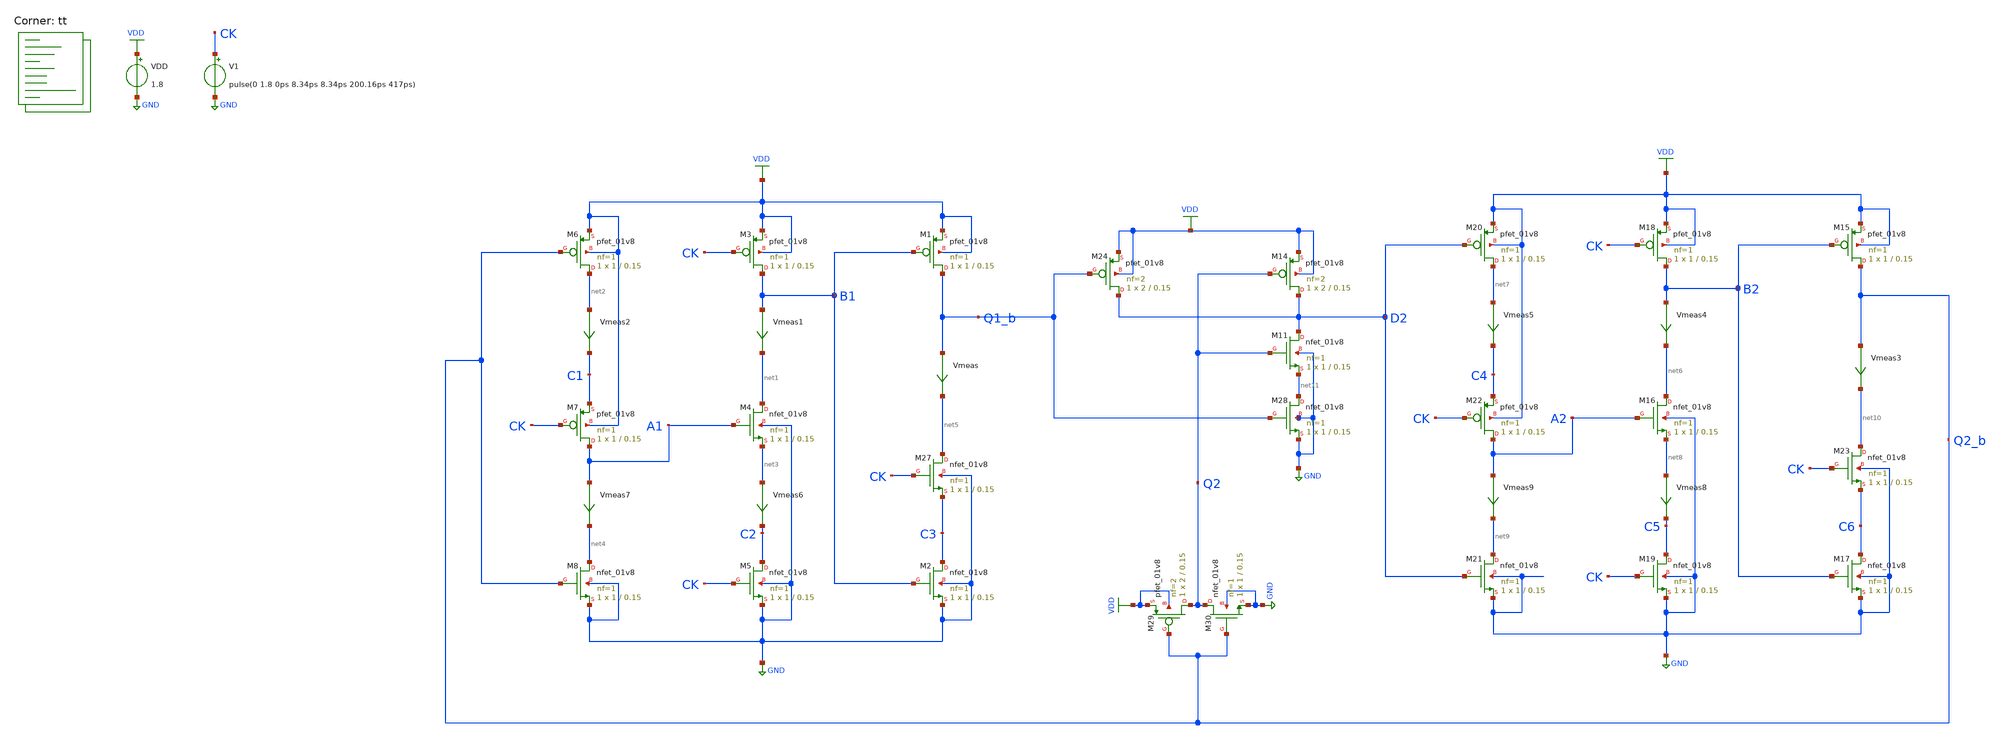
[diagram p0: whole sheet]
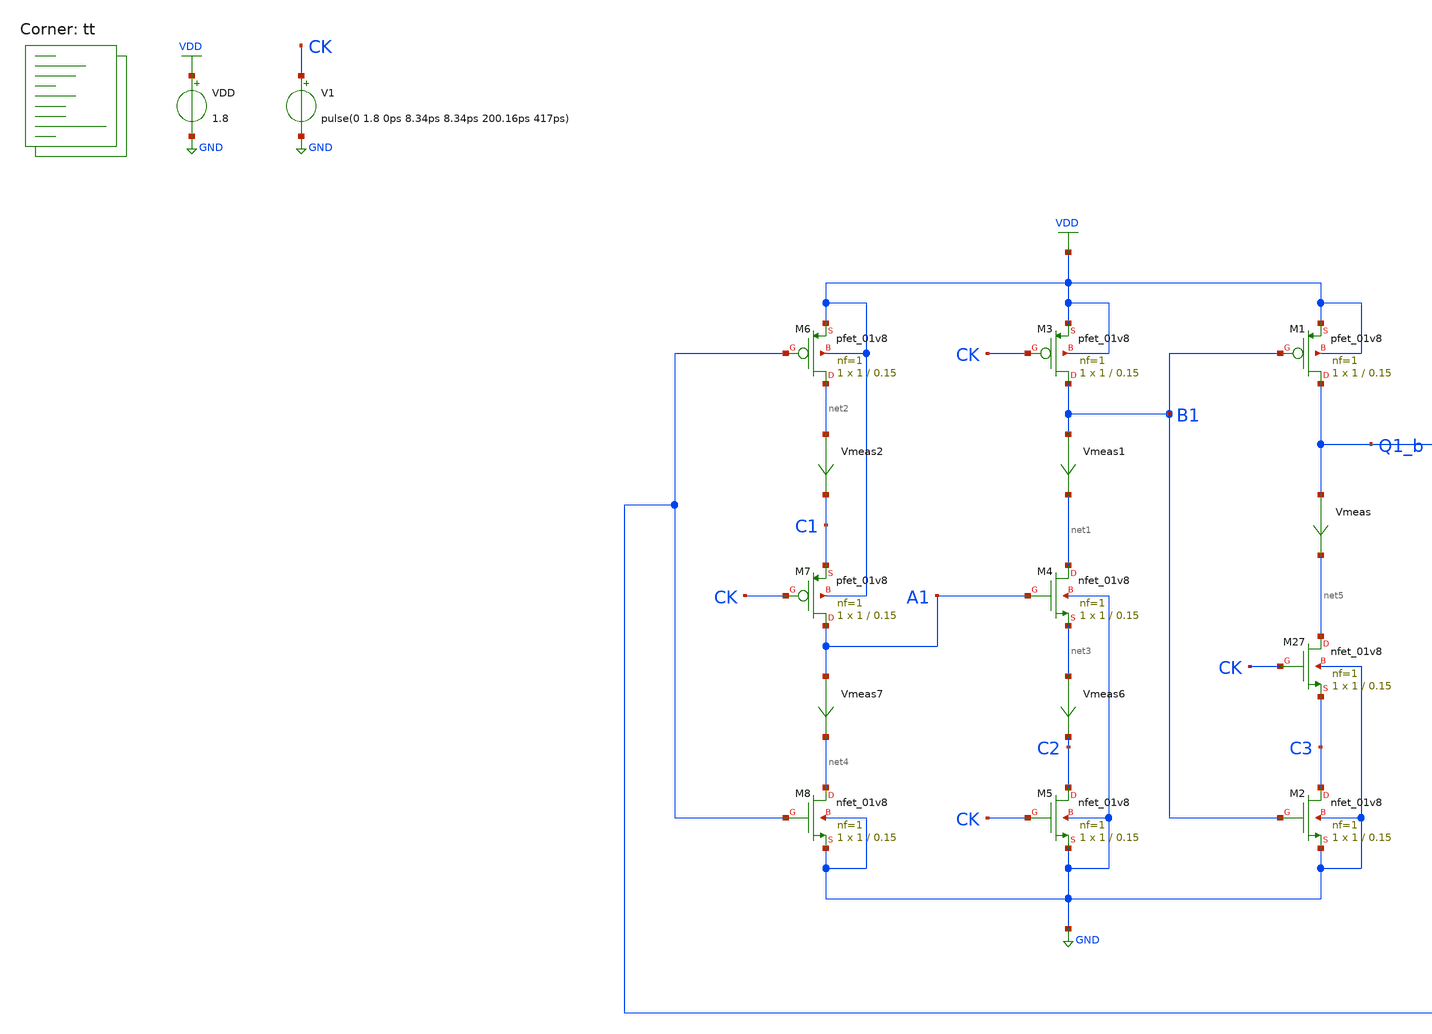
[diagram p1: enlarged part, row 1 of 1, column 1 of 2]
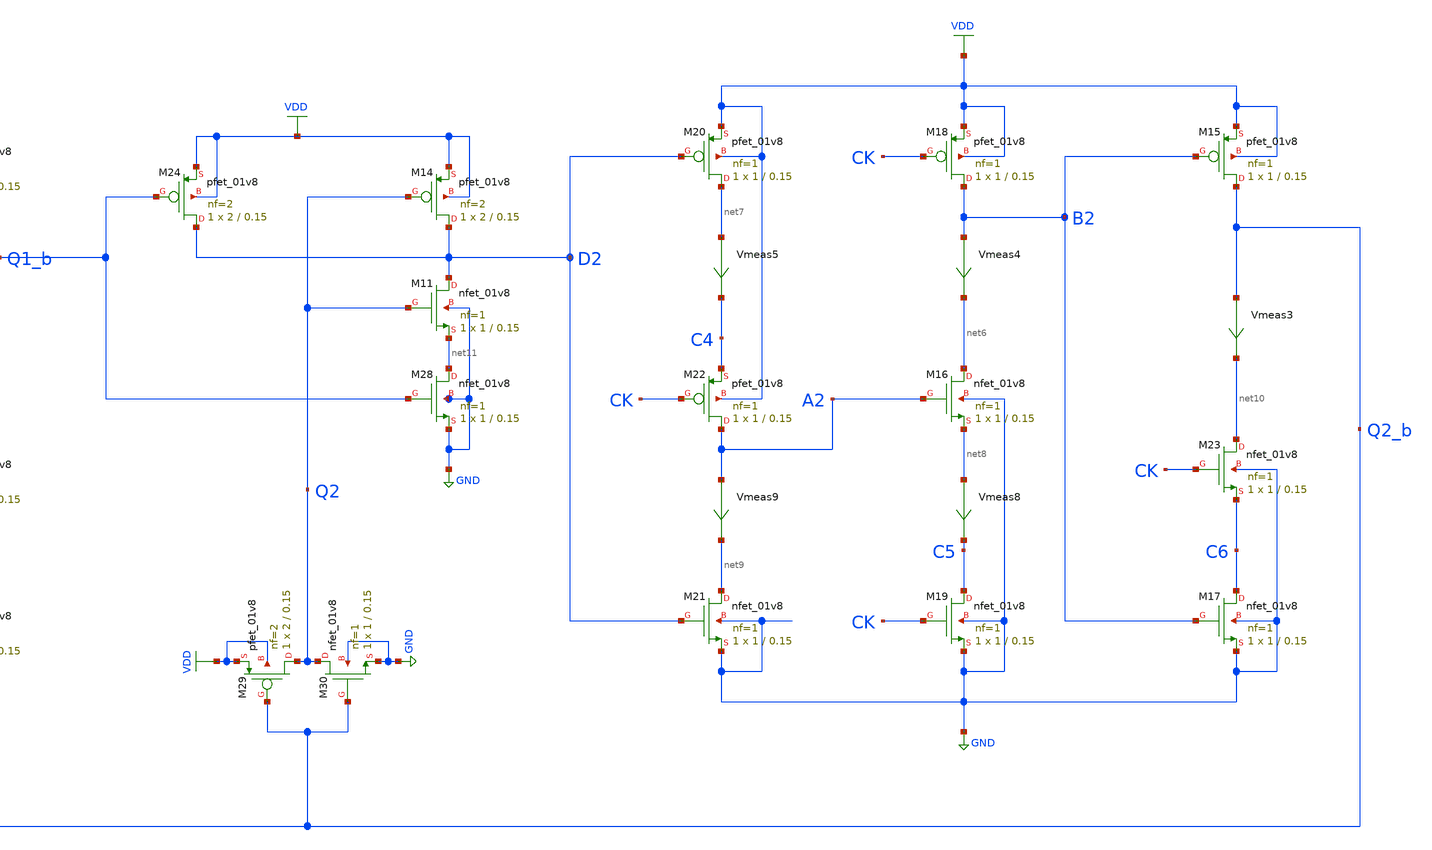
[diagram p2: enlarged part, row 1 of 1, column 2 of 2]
** sch_path: projects/pll/divider/xschem_ngspice/tb_TSPC_FF_divide3_2.sch
**.subckt tb_TSPC_FF_divide3_2
VDD VDD GND 1.8
XM1 Q1_b B1 VDD VDD sky130_fd_pr__pfet_01v8 L=0.15 W=1 nf=1 ad='int((nf+1)/2) * W/nf * 0.29' as='int((nf+2)/2) * W/nf * 0.29'
+ pd='2*int((nf+1)/2) * (W/nf + 0.29)' ps='2*int((nf+2)/2) * (W/nf + 0.29)' nrd='0.29 / W' nrs='0.29 / W'
+ sa=0 sb=0 sd=0 mult=1 m=1
XM4 net1 A1 net3 GND sky130_fd_pr__nfet_01v8 L=0.15 W=1 nf=1 ad='int((nf+1)/2) * W/nf * 0.29' as='int((nf+2)/2) * W/nf * 0.29'
+ pd='2*int((nf+1)/2) * (W/nf + 0.29)' ps='2*int((nf+2)/2) * (W/nf + 0.29)' nrd='0.29 / W' nrs='0.29 / W'
+ sa=0 sb=0 sd=0 mult=1 m=1
Vmeas Q1_b net5 0
.save i(vmeas)
XM2 C3 B1 GND GND sky130_fd_pr__nfet_01v8 L=0.15 W=1 nf=1 ad='int((nf+1)/2) * W/nf * 0.29' as='int((nf+2)/2) * W/nf * 0.29'
+ pd='2*int((nf+1)/2) * (W/nf + 0.29)' ps='2*int((nf+2)/2) * (W/nf + 0.29)' nrd='0.29 / W' nrs='0.29 / W'
+ sa=0 sb=0 sd=0 mult=1 m=1
XM3 B1 CK VDD VDD sky130_fd_pr__pfet_01v8 L=0.15 W=1 nf=1 ad='int((nf+1)/2) * W/nf * 0.29' as='int((nf+2)/2) * W/nf * 0.29'
+ pd='2*int((nf+1)/2) * (W/nf + 0.29)' ps='2*int((nf+2)/2) * (W/nf + 0.29)' nrd='0.29 / W' nrs='0.29 / W'
+ sa=0 sb=0 sd=0 mult=1 m=1
XM5 C2 CK GND GND sky130_fd_pr__nfet_01v8 L=0.15 W=1 nf=1 ad='int((nf+1)/2) * W/nf * 0.29' as='int((nf+2)/2) * W/nf * 0.29'
+ pd='2*int((nf+1)/2) * (W/nf + 0.29)' ps='2*int((nf+2)/2) * (W/nf + 0.29)' nrd='0.29 / W' nrs='0.29 / W'
+ sa=0 sb=0 sd=0 mult=1 m=1
Vmeas1 B1 net1 0
.save i(vmeas1)
XM6 net2 Q2_b VDD VDD sky130_fd_pr__pfet_01v8 L=0.15 W=1 nf=1 ad='int((nf+1)/2) * W/nf * 0.29' as='int((nf+2)/2) * W/nf * 0.29'
+ pd='2*int((nf+1)/2) * (W/nf + 0.29)' ps='2*int((nf+2)/2) * (W/nf + 0.29)' nrd='0.29 / W' nrs='0.29 / W'
+ sa=0 sb=0 sd=0 mult=1 m=1
XM8 net4 Q2_b GND GND sky130_fd_pr__nfet_01v8 L=0.15 W=1 nf=1 ad='int((nf+1)/2) * W/nf * 0.29' as='int((nf+2)/2) * W/nf * 0.29'
+ pd='2*int((nf+1)/2) * (W/nf + 0.29)' ps='2*int((nf+2)/2) * (W/nf + 0.29)' nrd='0.29 / W' nrs='0.29 / W'
+ sa=0 sb=0 sd=0 mult=1 m=1
Vmeas2 net2 C1 0
.save i(vmeas2)
XM7 A1 CK C1 VDD sky130_fd_pr__pfet_01v8 L=0.15 W=1 nf=1 ad='int((nf+1)/2) * W/nf * 0.29' as='int((nf+2)/2) * W/nf * 0.29'
+ pd='2*int((nf+1)/2) * (W/nf + 0.29)' ps='2*int((nf+2)/2) * (W/nf + 0.29)' nrd='0.29 / W' nrs='0.29 / W'
+ sa=0 sb=0 sd=0 mult=1 m=1
Vmeas6 net3 C2 0
.save i(vmeas6)
Vmeas7 A1 net4 0
.save i(vmeas7)
XM27 net5 CK C3 GND sky130_fd_pr__nfet_01v8 L=0.15 W=1 nf=1 ad='int((nf+1)/2) * W/nf * 0.29' as='int((nf+2)/2) * W/nf * 0.29'
+ pd='2*int((nf+1)/2) * (W/nf + 0.29)' ps='2*int((nf+2)/2) * (W/nf + 0.29)' nrd='0.29 / W' nrs='0.29 / W'
+ sa=0 sb=0 sd=0 mult=1 m=1
XM15 Q2_b B2 VDD VDD sky130_fd_pr__pfet_01v8 L=0.15 W=1 nf=1 ad='int((nf+1)/2) * W/nf * 0.29' as='int((nf+2)/2) * W/nf * 0.29'
+ pd='2*int((nf+1)/2) * (W/nf + 0.29)' ps='2*int((nf+2)/2) * (W/nf + 0.29)' nrd='0.29 / W' nrs='0.29 / W'
+ sa=0 sb=0 sd=0 mult=1 m=1
XM16 net6 A2 net8 GND sky130_fd_pr__nfet_01v8 L=0.15 W=1 nf=1 ad='int((nf+1)/2) * W/nf * 0.29' as='int((nf+2)/2) * W/nf * 0.29'
+ pd='2*int((nf+1)/2) * (W/nf + 0.29)' ps='2*int((nf+2)/2) * (W/nf + 0.29)' nrd='0.29 / W' nrs='0.29 / W'
+ sa=0 sb=0 sd=0 mult=1 m=1
Vmeas3 Q2_b net10 0
.save i(vmeas3)
XM17 C6 B2 GND GND sky130_fd_pr__nfet_01v8 L=0.15 W=1 nf=1 ad='int((nf+1)/2) * W/nf * 0.29' as='int((nf+2)/2) * W/nf * 0.29'
+ pd='2*int((nf+1)/2) * (W/nf + 0.29)' ps='2*int((nf+2)/2) * (W/nf + 0.29)' nrd='0.29 / W' nrs='0.29 / W'
+ sa=0 sb=0 sd=0 mult=1 m=1
XM18 B2 CK VDD VDD sky130_fd_pr__pfet_01v8 L=0.15 W=1 nf=1 ad='int((nf+1)/2) * W/nf * 0.29' as='int((nf+2)/2) * W/nf * 0.29'
+ pd='2*int((nf+1)/2) * (W/nf + 0.29)' ps='2*int((nf+2)/2) * (W/nf + 0.29)' nrd='0.29 / W' nrs='0.29 / W'
+ sa=0 sb=0 sd=0 mult=1 m=1
XM19 C5 CK GND GND sky130_fd_pr__nfet_01v8 L=0.15 W=1 nf=1 ad='int((nf+1)/2) * W/nf * 0.29' as='int((nf+2)/2) * W/nf * 0.29'
+ pd='2*int((nf+1)/2) * (W/nf + 0.29)' ps='2*int((nf+2)/2) * (W/nf + 0.29)' nrd='0.29 / W' nrs='0.29 / W'
+ sa=0 sb=0 sd=0 mult=1 m=1
Vmeas4 B2 net6 0
.save i(vmeas4)
XM20 net7 D2 VDD VDD sky130_fd_pr__pfet_01v8 L=0.15 W=1 nf=1 ad='int((nf+1)/2) * W/nf * 0.29' as='int((nf+2)/2) * W/nf * 0.29'
+ pd='2*int((nf+1)/2) * (W/nf + 0.29)' ps='2*int((nf+2)/2) * (W/nf + 0.29)' nrd='0.29 / W' nrs='0.29 / W'
+ sa=0 sb=0 sd=0 mult=1 m=1
XM21 net9 D2 GND GND sky130_fd_pr__nfet_01v8 L=0.15 W=1 nf=1 ad='int((nf+1)/2) * W/nf * 0.29' as='int((nf+2)/2) * W/nf * 0.29'
+ pd='2*int((nf+1)/2) * (W/nf + 0.29)' ps='2*int((nf+2)/2) * (W/nf + 0.29)' nrd='0.29 / W' nrs='0.29 / W'
+ sa=0 sb=0 sd=0 mult=1 m=1
Vmeas5 net7 C4 0
.save i(vmeas5)
XM22 A2 CK C4 VDD sky130_fd_pr__pfet_01v8 L=0.15 W=1 nf=1 ad='int((nf+1)/2) * W/nf * 0.29' as='int((nf+2)/2) * W/nf * 0.29'
+ pd='2*int((nf+1)/2) * (W/nf + 0.29)' ps='2*int((nf+2)/2) * (W/nf + 0.29)' nrd='0.29 / W' nrs='0.29 / W'
+ sa=0 sb=0 sd=0 mult=1 m=1
Vmeas8 net8 C5 0
.save i(vmeas8)
Vmeas9 A2 net9 0
.save i(vmeas9)
XM23 net10 CK C6 GND sky130_fd_pr__nfet_01v8 L=0.15 W=1 nf=1 ad='int((nf+1)/2) * W/nf * 0.29' as='int((nf+2)/2) * W/nf * 0.29'
+ pd='2*int((nf+1)/2) * (W/nf + 0.29)' ps='2*int((nf+2)/2) * (W/nf + 0.29)' nrd='0.29 / W' nrs='0.29 / W'
+ sa=0 sb=0 sd=0 mult=1 m=1
V1 CK GND pulse(0 1.8 0ps 8.34ps 8.34ps 200.16ps 417ps)
XM11 D2 Q2 net11 GND sky130_fd_pr__nfet_01v8 L=0.15 W=1 nf=1 ad='int((nf+1)/2) * W/nf * 0.29' as='int((nf+2)/2) * W/nf * 0.29'
+ pd='2*int((nf+1)/2) * (W/nf + 0.29)' ps='2*int((nf+2)/2) * (W/nf + 0.29)' nrd='0.29 / W' nrs='0.29 / W'
+ sa=0 sb=0 sd=0 mult=1 m=1
XM14 D2 Q2 VDD VDD sky130_fd_pr__pfet_01v8 L=0.15 W=2 nf=2 ad='int((nf+1)/2) * W/nf * 0.29' as='int((nf+2)/2) * W/nf * 0.29'
+ pd='2*int((nf+1)/2) * (W/nf + 0.29)' ps='2*int((nf+2)/2) * (W/nf + 0.29)' nrd='0.29 / W' nrs='0.29 / W'
+ sa=0 sb=0 sd=0 mult=1 m=1
XM24 D2 Q1_b VDD VDD sky130_fd_pr__pfet_01v8 L=0.15 W=2 nf=2 ad='int((nf+1)/2) * W/nf * 0.29' as='int((nf+2)/2) * W/nf * 0.29'
+ pd='2*int((nf+1)/2) * (W/nf + 0.29)' ps='2*int((nf+2)/2) * (W/nf + 0.29)' nrd='0.29 / W' nrs='0.29 / W'
+ sa=0 sb=0 sd=0 mult=1 m=1
XM28 net11 Q1_b GND GND sky130_fd_pr__nfet_01v8 L=0.15 W=1 nf=1 ad='int((nf+1)/2) * W/nf * 0.29' as='int((nf+2)/2) * W/nf * 0.29'
+ pd='2*int((nf+1)/2) * (W/nf + 0.29)' ps='2*int((nf+2)/2) * (W/nf + 0.29)' nrd='0.29 / W' nrs='0.29 / W'
+ sa=0 sb=0 sd=0 mult=1 m=1
XM29 Q2 Q2_b VDD VDD sky130_fd_pr__pfet_01v8 L=0.15 W=2 nf=2 ad='int((nf+1)/2) * W/nf * 0.29' as='int((nf+2)/2) * W/nf * 0.29'
+ pd='2*int((nf+1)/2) * (W/nf + 0.29)' ps='2*int((nf+2)/2) * (W/nf + 0.29)' nrd='0.29 / W' nrs='0.29 / W'
+ sa=0 sb=0 sd=0 mult=1 m=1
XM30 Q2 Q2_b GND GND sky130_fd_pr__nfet_01v8 L=0.15 W=1 nf=1 ad='int((nf+1)/2) * W/nf * 0.29' as='int((nf+2)/2) * W/nf * 0.29'
+ pd='2*int((nf+1)/2) * (W/nf + 0.29)' ps='2*int((nf+2)/2) * (W/nf + 0.29)' nrd='0.29 / W' nrs='0.29 / W'
+ sa=0 sb=0 sd=0 mult=1 m=1
**** begin user architecture code



.include /foss/pdks/sky130A/libs.ref/sky130_fd_sc_hd/spice/sky130_fd_sc_hd.spice


.save @m.xm1.msky130_fd_pr__pfet_01v8[gm] @m.xm27.msky130_fd_pr__nfet_01v8[gm] @m.xm2.msky130_fd_pr__nfet_01v8[gm] @m.xm3.msky130_fd_pr__pfet_01v8[gm] @m.xm4.msky130_fd_pr__nfet_01v8[gm] @m.xm5.msky130_fd_pr__nfet_01v8[gm] @m.xm6.msky130_fd_pr__pfet_01v8[gm] @m.xm7.msky130_fd_pr__pfet_01v8[gm] @m.xm8.msky130_fd_pr__nfet_01v8[gm]

.option method=gear
.option wnflag=1
.option savecurrents


*.ic v(d)=0
.ic v(q1_b)=1.8
.ic v(q2_b)=1.8

.control

  save v(d1) v(d2) v(q1) v(q2) v(q1_b) v(q2_b) v(q3) v(q4) v(q3_b) v(q4_b) v(a1) v(a2) v(a3) v(a4)
+ v(b1) v(b2) v(b3) v(b4) v(c1) v(c2) v(c3) v(c4) v(c5) v(c6) v(c7) v(c8) v(ck) v(ck1) v(ck1_b)
  * save all
  * tran 0.1n 1u
  tran 1p 20n

  remzerovec
  write tb_TSPC_FF_divide3_2.raw
  * set appendwrite

.endc



.lib $::SKYWATER_MODELS/sky130.lib.spice tt
**** end user architecture code
**.ends
.GLOBAL GND
.GLOBAL VDD
.end
